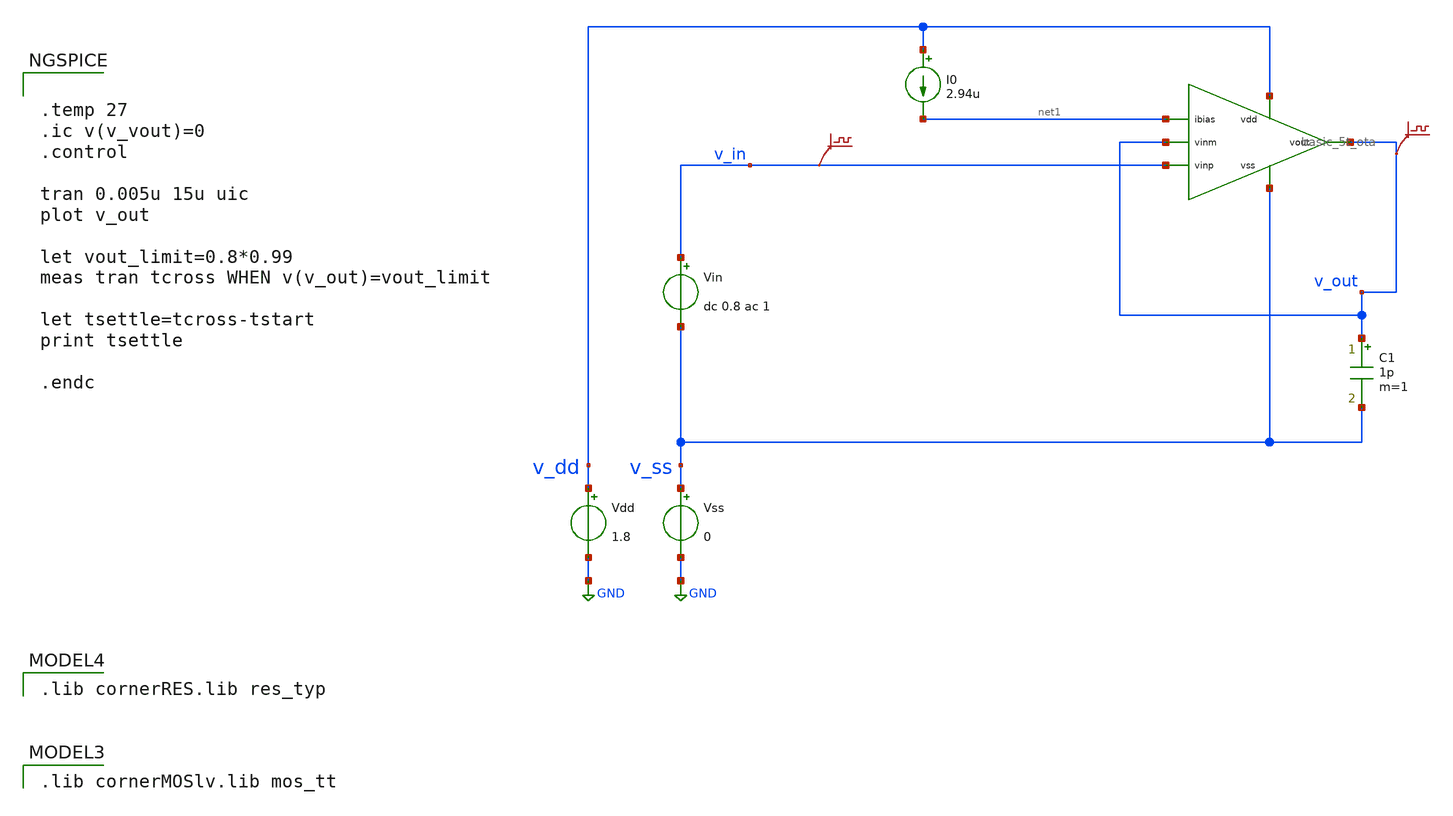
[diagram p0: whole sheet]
** sch_path: design/ota_design/basic_5t_ota_tran.sch
**.subckt basic_5t_ota_tran
Vdd v_dd GND 1.8
Vss v_ss GND 0
C1 v_out v_ss 1p m=1
Vin v_in v_ss dc 0.8 ac 1
I0 v_dd net1 2.94u
.save v(v_in)
.save v(v_out)
x1 v_dd v_out net1 v_out v_in v_ss basic_5t_ota
**** begin user architecture code
 .lib cornerMOSlv.lib mos_tt

 .lib cornerRES.lib res_typ



.temp 27
.ic v(v_vout)=0
.control

tran 0.005u 15u uic
plot v_out

let vout_limit=0.8*0.99
meas tran tcross WHEN v(v_out)=vout_limit

let tsettle=tcross-tstart
print tsettle

.endc


**** end user architecture code
**.ends
.GLOBAL GND
.end
